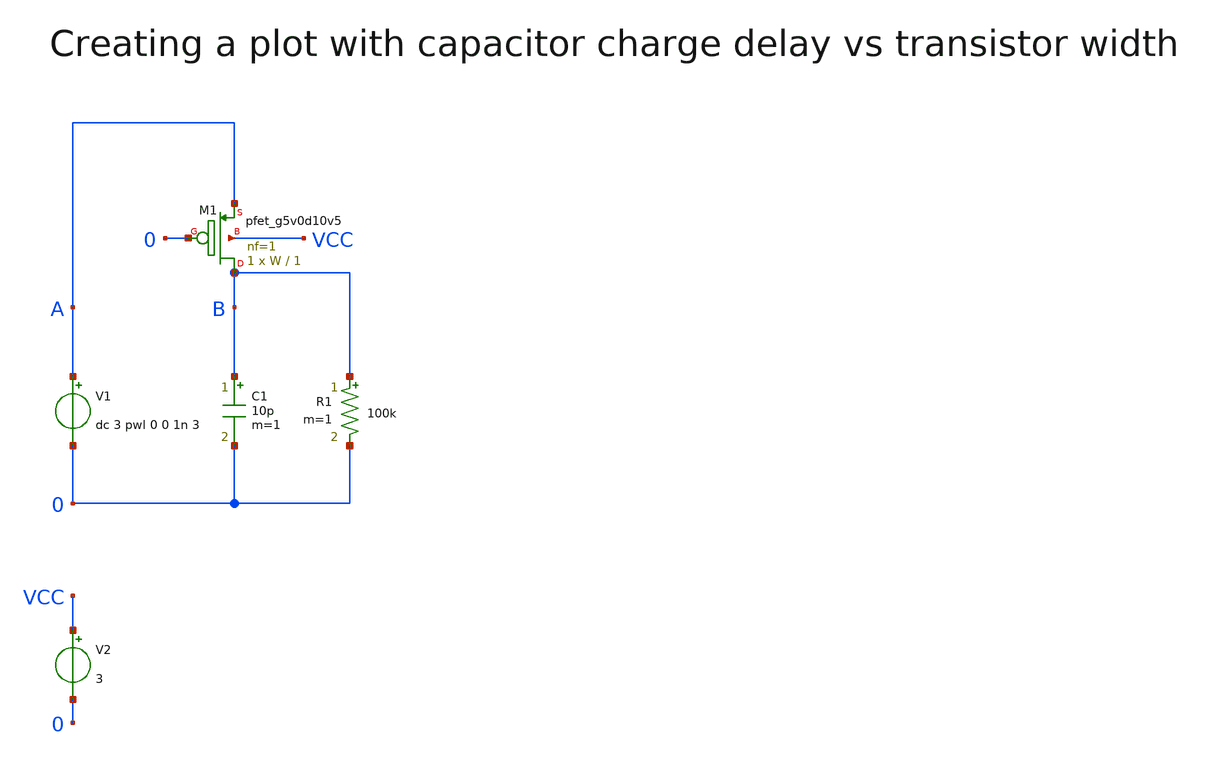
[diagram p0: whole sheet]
** sch_path: sky130A/xschem_libs/sky130_tests_ase/test_customplot/schematic/test_customplot.sch
**.subckt test_customplot
V1 A 0 dc 3 pwl 0 0 1n 3
C1 B 0 10p m=1
XM1 B 0 A VCC sky130_fd_pr__pfet_g5v0d10v5 L=1 W=W nf=1 ad='int((1 + 1)/2) * W / 1 * 0.29' as='int((1 + 2)/2) * W / 1 * 0.29'
+ pd='2*int((1 + 1)/2) * (W / 1 + 0.29)' ps='2*int((1 + 2)/2) * (W / 1 + 0.29)' nrd='0.29 / W ' nrs='0.29 / W '
+ sa=0 sb=0 sd=0 mult=1 m=1
V2 VCC 0 3
R1 B 0 100k m=1
**.ends
.end
